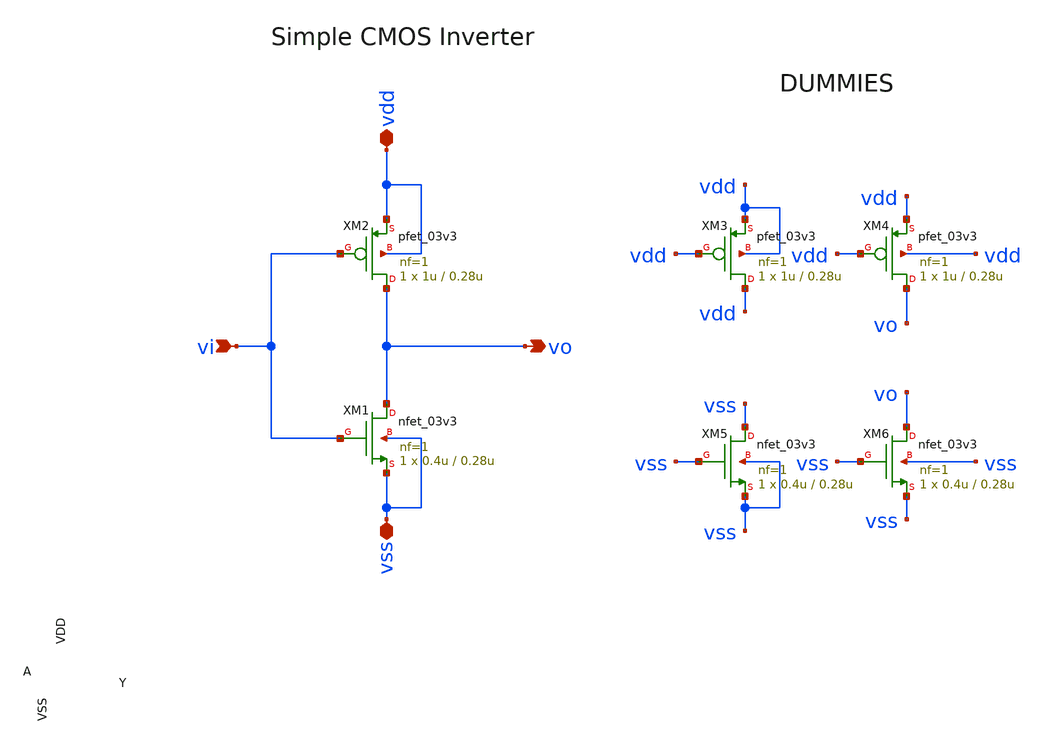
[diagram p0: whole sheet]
** sch_path: Analog/schematics/3_comparator/inv.sch
**.subckt inv vdd vss vi vo
*.iopin vdd
*.iopin vss
*.ipin vi
*.opin vo
XM1 vo vi vss vss nfet_03v3 L=0.28u W=0.4u nf=1 ad='int((nf+1)/2) * W/nf * 0.18u' as='int((nf+2)/2) * W/nf * 0.18u'
+ pd='2*int((nf+1)/2) * (W/nf + 0.18u)' ps='2*int((nf+2)/2) * (W/nf + 0.18u)' nrd='0.18u / W' nrs='0.18u / W'
+ sa=0 sb=0 sd=0 m=1
XM2 vo vi vdd vdd pfet_03v3 L=0.28u W=1u nf=1 ad='int((nf+1)/2) * W/nf * 0.18u' as='int((nf+2)/2) * W/nf * 0.18u'
+ pd='2*int((nf+1)/2) * (W/nf + 0.18u)' ps='2*int((nf+2)/2) * (W/nf + 0.18u)' nrd='0.18u / W' nrs='0.18u / W'
+ sa=0 sb=0 sd=0 m=1
XM3 vdd vdd vdd vdd pfet_03v3 L=0.28u W=1u nf=1 ad='int((nf+1)/2) * W/nf * 0.18u' as='int((nf+2)/2) * W/nf * 0.18u'
+ pd='2*int((nf+1)/2) * (W/nf + 0.18u)' ps='2*int((nf+2)/2) * (W/nf + 0.18u)' nrd='0.18u / W' nrs='0.18u / W'
+ sa=0 sb=0 sd=0 m=1
XM4 vo vdd vdd vdd pfet_03v3 L=0.28u W=1u nf=1 ad='int((nf+1)/2) * W/nf * 0.18u' as='int((nf+2)/2) * W/nf * 0.18u'
+ pd='2*int((nf+1)/2) * (W/nf + 0.18u)' ps='2*int((nf+2)/2) * (W/nf + 0.18u)' nrd='0.18u / W' nrs='0.18u / W'
+ sa=0 sb=0 sd=0 m=1
XM5 vss vss vss vss nfet_03v3 L=0.28u W=0.4u nf=1 ad='int((nf+1)/2) * W/nf * 0.18u' as='int((nf+2)/2) * W/nf * 0.18u'
+ pd='2*int((nf+1)/2) * (W/nf + 0.18u)' ps='2*int((nf+2)/2) * (W/nf + 0.18u)' nrd='0.18u / W' nrs='0.18u / W'
+ sa=0 sb=0 sd=0 m=1
XM6 vo vss vss vss nfet_03v3 L=0.28u W=0.4u nf=1 ad='int((nf+1)/2) * W/nf * 0.18u' as='int((nf+2)/2) * W/nf * 0.18u'
+ pd='2*int((nf+1)/2) * (W/nf + 0.18u)' ps='2*int((nf+2)/2) * (W/nf + 0.18u)' nrd='0.18u / W' nrs='0.18u / W'
+ sa=0 sb=0 sd=0 m=1
**.ends
.end
